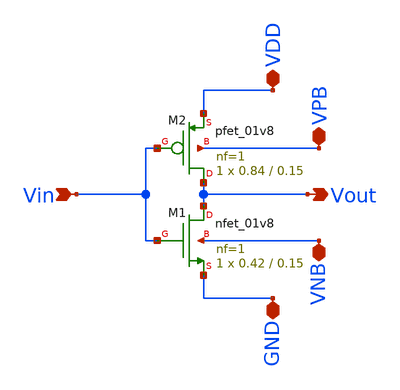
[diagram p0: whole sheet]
** sch_path: INV.sch
**.subckt INV Vin GND VDD Vout VPB VNB
*.ipin Vin
*.iopin GND
*.iopin VDD
*.opin Vout
*.iopin VPB
*.iopin VNB
XM1 Vout Vin GND VNB sky130_fd_pr__nfet_01v8 L=0.15 W=0.42 nf=1 ad=0.1218 as=0.1218 pd=1.42 ps=1.42
+ nrd=0.690476 nrs=0.690476 sa=0 sb=0 sd=0 mult=1 m=1
XM2 Vout Vin VDD VPB sky130_fd_pr__pfet_01v8 L=0.15 W=0.84 nf=1 ad=0.2436 as=0.2436 pd=2.26 ps=2.26
+ nrd=0.345238 nrs=0.345238 sa=0 sb=0 sd=0 mult=1 m=1
**.ends
.end
